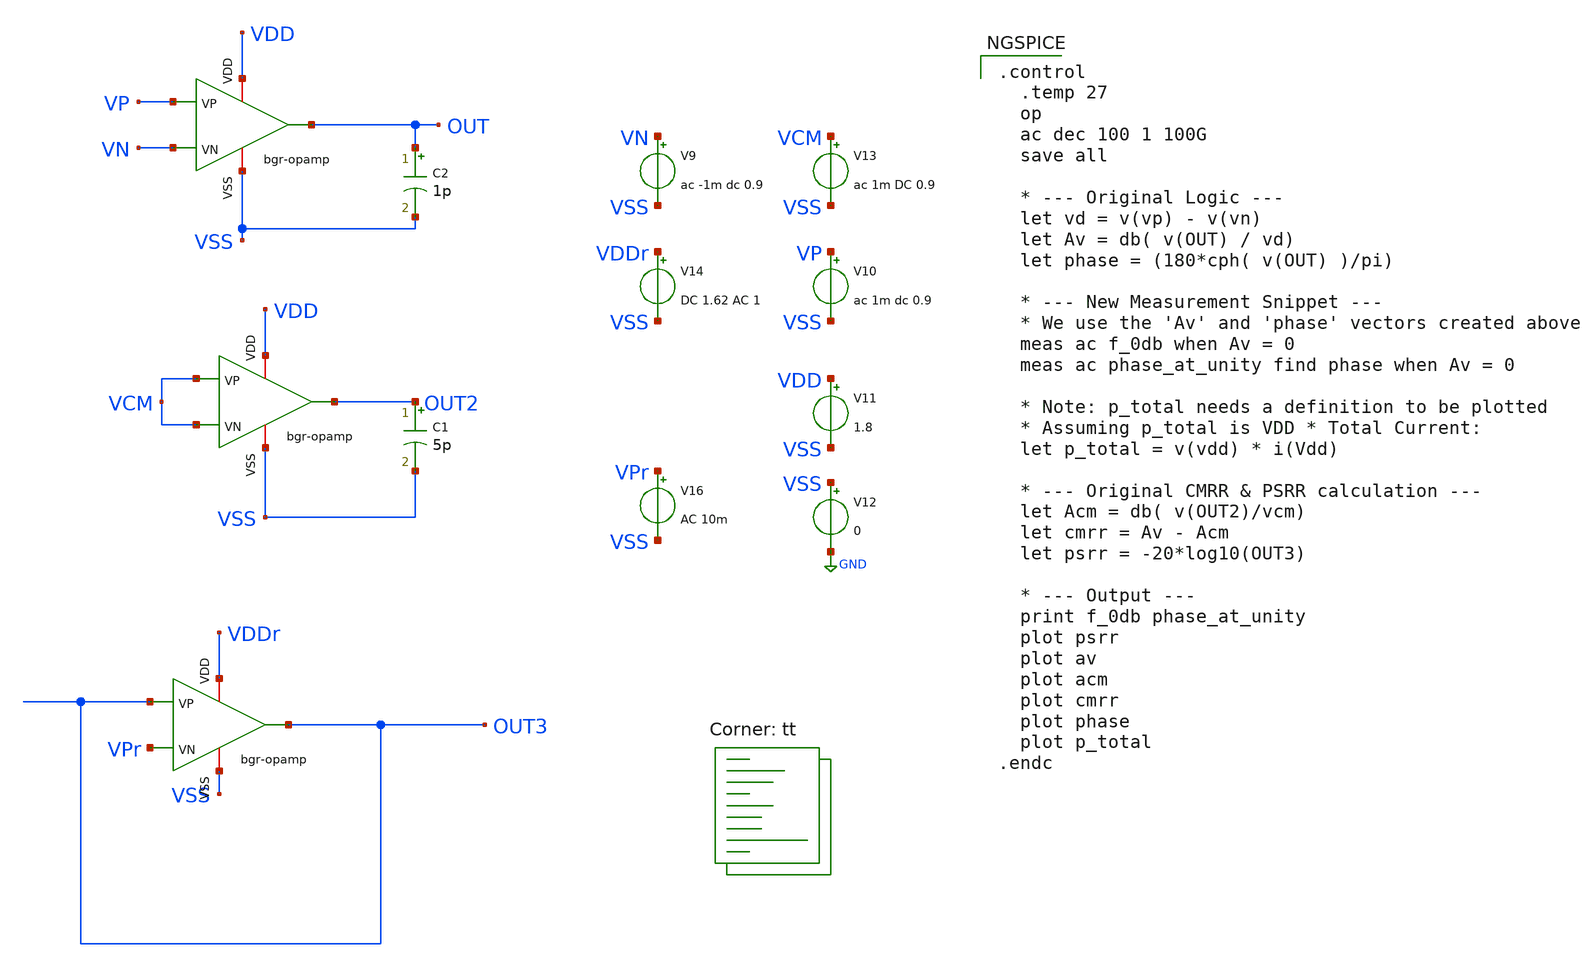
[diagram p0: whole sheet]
** sch_path: bandgap/bgr-opamp/tb_ac.sch
**.subckt tb_ac
C2 OUT VSS 1p m=1
C1 OUT2 VSS 5p m=1
x1 VDD OUT VP VN VSS bgr-opamp
x2 VDD OUT2 VCM VCM VSS bgr-opamp
x3 VDDr OUT3 OUT3 VPr VSS bgr-opamp
V9 VN VSS ac -1m dc 0.9
V10 VP VSS ac 1m dc 0.9
V11 VDD VSS 1.8
V12 VSS GND 0
V13 VCM VSS ac 1m DC 0.9
V14 VDDr VSS DC 1.62 AC 1
V16 VPr VSS AC 10m
**** begin user architecture code

.control
  .temp 27
  op
  ac dec 100 1 100G
  save all

  * --- Original Logic ---
  let vd = v(vp) - v(vn)
  let Av = db( v(OUT) / vd)
  let phase = (180*cph( v(OUT) )/pi)

  * --- New Measurement Snippet ---
  * We use the 'Av' and 'phase' vectors created above
  meas ac f_0db when Av = 0
  meas ac phase_at_unity find phase when Av = 0

  * Note: p_total needs a definition to be plotted
  * Assuming p_total is VDD * Total Current:
  let p_total = v(vdd) * i(Vdd)

  * --- Original CMRR & PSRR calculation ---
  let Acm = db( v(OUT2)/vcm)
  let cmrr = Av - Acm
  let psrr = -20*log10(OUT3)

  * --- Output ---
  print f_0db phase_at_unity
  plot psrr
  plot av
  plot acm
  plot cmrr
  plot phase
  plot p_total
.endc



.lib $::SKYWATER_MODELS/sky130.lib.spice tt
**** end user architecture code
**.ends

* expanding   symbol:  afe-icdec-teknofest-2026/bandgap/bgr-opamp/bgr-opamp.sym # of pins=5
** sym_path: bandgap/bgr-opamp/bgr-opamp.sym
** sch_path: bandgap/bgr-opamp/bgr-opamp.sch
.subckt bgr-opamp VDD OUT VP VN VSS
*.iopin VSS
*.iopin VDD
*.ipin VP
*.ipin VN
*.opin OUT
XM2 net2 VN net3 VSS sky130_fd_pr__nfet_01v8 L=0.3 W=30 nf=2 ad='int((nf+1)/2) * W/nf * 0.29' as='int((nf+2)/2) * W/nf * 0.29'
+ pd='2*int((nf+1)/2) * (W/nf + 0.29)' ps='2*int((nf+2)/2) * (W/nf + 0.29)' nrd='0.29 / W' nrs='0.29 / W'
+ sa=0 sb=0 sd=0 mult=1 m=1
XM4 net2 net1 VDD VDD sky130_fd_pr__pfet_01v8 L=1.25 W=10.8 nf=4 ad='int((nf+1)/2) * W/nf * 0.29' as='int((nf+2)/2) * W/nf * 0.29'
+ pd='2*int((nf+1)/2) * (W/nf + 0.29)' ps='2*int((nf+2)/2) * (W/nf + 0.29)' nrd='0.29 / W' nrs='0.29 / W'
+ sa=0 sb=0 sd=0 mult=1 m=1
XM3 net1 net1 VDD VDD sky130_fd_pr__pfet_01v8 L=1.25 W=10.8 nf=4 ad='int((nf+1)/2) * W/nf * 0.29' as='int((nf+2)/2) * W/nf * 0.29'
+ pd='2*int((nf+1)/2) * (W/nf + 0.29)' ps='2*int((nf+2)/2) * (W/nf + 0.29)' nrd='0.29 / W' nrs='0.29 / W'
+ sa=0 sb=0 sd=0 mult=1 m=1
XM5 net3 net11 VSS VSS sky130_fd_pr__nfet_01v8 L=1.25 W=3.4 nf=1 ad='int((nf+1)/2) * W/nf * 0.29' as='int((nf+2)/2) * W/nf * 0.29'
+ pd='2*int((nf+1)/2) * (W/nf + 0.29)' ps='2*int((nf+2)/2) * (W/nf + 0.29)' nrd='0.29 / W' nrs='0.29 / W'
+ sa=0 sb=0 sd=0 mult=1 m=1
XM9 net4 net5 net12 VSS sky130_fd_pr__nfet_01v8 L=1.25 W=13.6 nf=1 ad='int((nf+1)/2) * W/nf * 0.29' as='int((nf+2)/2) * W/nf * 0.29'
+ pd='2*int((nf+1)/2) * (W/nf + 0.29)' ps='2*int((nf+2)/2) * (W/nf + 0.29)' nrd='0.29 / W' nrs='0.29 / W'
+ sa=0 sb=0 sd=0 mult=1 m=1
XM8 net4 net4 VDD VDD sky130_fd_pr__pfet_01v8 L=1.25 W=10.8 nf=4 ad='int((nf+1)/2) * W/nf * 0.29' as='int((nf+2)/2) * W/nf * 0.29'
+ pd='2*int((nf+1)/2) * (W/nf + 0.29)' ps='2*int((nf+2)/2) * (W/nf + 0.29)' nrd='0.29 / W' nrs='0.29 / W'
+ sa=0 sb=0 sd=0 mult=1 m=1
XM11 net5 net4 VDD VDD sky130_fd_pr__pfet_01v8 L=1.25 W=10.8 nf=4 ad='int((nf+1)/2) * W/nf * 0.29' as='int((nf+2)/2) * W/nf * 0.29'
+ pd='2*int((nf+1)/2) * (W/nf + 0.29)' ps='2*int((nf+2)/2) * (W/nf + 0.29)' nrd='0.29 / W' nrs='0.29 / W'
+ sa=0 sb=0 sd=0 mult=1 m=1
XM10 net5 net5 net6 net6 sky130_fd_pr__nfet_01v8 L=1.25 W=3.4 nf=1 ad='int((nf+1)/2) * W/nf * 0.29' as='int((nf+2)/2) * W/nf * 0.29'
+ pd='2*int((nf+1)/2) * (W/nf + 0.29)' ps='2*int((nf+2)/2) * (W/nf + 0.29)' nrd='0.29 / W' nrs='0.29 / W'
+ sa=0 sb=0 sd=0 mult=1 m=1
XM6 OUT net2 VDD VDD sky130_fd_pr__pfet_01v8 L=1.25 W=100 nf=32 ad='int((nf+1)/2) * W/nf * 0.29' as='int((nf+2)/2) * W/nf * 0.29'
+ pd='2*int((nf+1)/2) * (W/nf + 0.29)' ps='2*int((nf+2)/2) * (W/nf + 0.29)' nrd='0.29 / W' nrs='0.29 / W'
+ sa=0 sb=0 sd=0 mult=1 m=1
XM7 OUT net11 VSS VSS sky130_fd_pr__nfet_01v8 L=1.25 W=14 nf=4 ad='int((nf+1)/2) * W/nf * 0.29' as='int((nf+2)/2) * W/nf * 0.29'
+ pd='2*int((nf+1)/2) * (W/nf + 0.29)' ps='2*int((nf+2)/2) * (W/nf + 0.29)' nrd='0.29 / W' nrs='0.29 / W'
+ sa=0 sb=0 sd=0 mult=1 m=1
XC2 OUT net2 sky130_fd_pr__cap_mim_m3_1 W=25 L=25 MF=32 m=32
XR2 net7 net12 VSS sky130_fd_pr__res_high_po_1p41 L=3.235 mult=1 m=1
XR3 net9 net7 VSS sky130_fd_pr__res_high_po_1p41 L=3.235 mult=1 m=1
XR4 net8 net9 VSS sky130_fd_pr__res_high_po_1p41 L=3.235 mult=1 m=1
XR5 net10 net8 VSS sky130_fd_pr__res_high_po_1p41 L=3.235 mult=1 m=1
XR6 VSS net10 VSS sky130_fd_pr__res_high_po_1p41 L=3.235 mult=1 m=1
XM13 net11 net4 VDD VDD sky130_fd_pr__pfet_01v8 L=1.25 W=10.8 nf=4 ad='int((nf+1)/2) * W/nf * 0.29' as='int((nf+2)/2) * W/nf * 0.29'
+ pd='2*int((nf+1)/2) * (W/nf + 0.29)' ps='2*int((nf+2)/2) * (W/nf + 0.29)' nrd='0.29 / W' nrs='0.29 / W'
+ sa=0 sb=0 sd=0 mult=1 m=1
XM14 net11 net11 VSS VSS sky130_fd_pr__nfet_01v8 L=1.25 W=6.8 nf=1 ad='int((nf+1)/2) * W/nf * 0.29' as='int((nf+2)/2) * W/nf * 0.29'
+ pd='2*int((nf+1)/2) * (W/nf + 0.29)' ps='2*int((nf+2)/2) * (W/nf + 0.29)' nrd='0.29 / W' nrs='0.29 / W'
+ sa=0 sb=0 sd=0 mult=1 m=1
XM15 net6 net6 VSS VSS sky130_fd_pr__nfet_01v8 L=1.25 W=3.4 nf=1 ad='int((nf+1)/2) * W/nf * 0.29' as='int((nf+2)/2) * W/nf * 0.29'
+ pd='2*int((nf+1)/2) * (W/nf + 0.29)' ps='2*int((nf+2)/2) * (W/nf + 0.29)' nrd='0.29 / W' nrs='0.29 / W'
+ sa=0 sb=0 sd=0 mult=1 m=1
XM12 net5 net4 net4 VSS sky130_fd_pr__pfet_01v8 L=0.15 W=0.85 nf=1 ad='int((nf+1)/2) * W/nf * 0.29' as='int((nf+2)/2) * W/nf * 0.29'
+ pd='2*int((nf+1)/2) * (W/nf + 0.29)' ps='2*int((nf+2)/2) * (W/nf + 0.29)' nrd='0.29 / W' nrs='0.29 / W'
+ sa=0 sb=0 sd=0 mult=1 m=1
XM16 net1 VP net3 VSS sky130_fd_pr__nfet_01v8 L=0.3 W=30 nf=2 ad='int((nf+1)/2) * W/nf * 0.29' as='int((nf+2)/2) * W/nf * 0.29'
+ pd='2*int((nf+1)/2) * (W/nf + 0.29)' ps='2*int((nf+2)/2) * (W/nf + 0.29)' nrd='0.29 / W' nrs='0.29 / W'
+ sa=0 sb=0 sd=0 mult=1 m=1
.ends

.GLOBAL GND
.end
